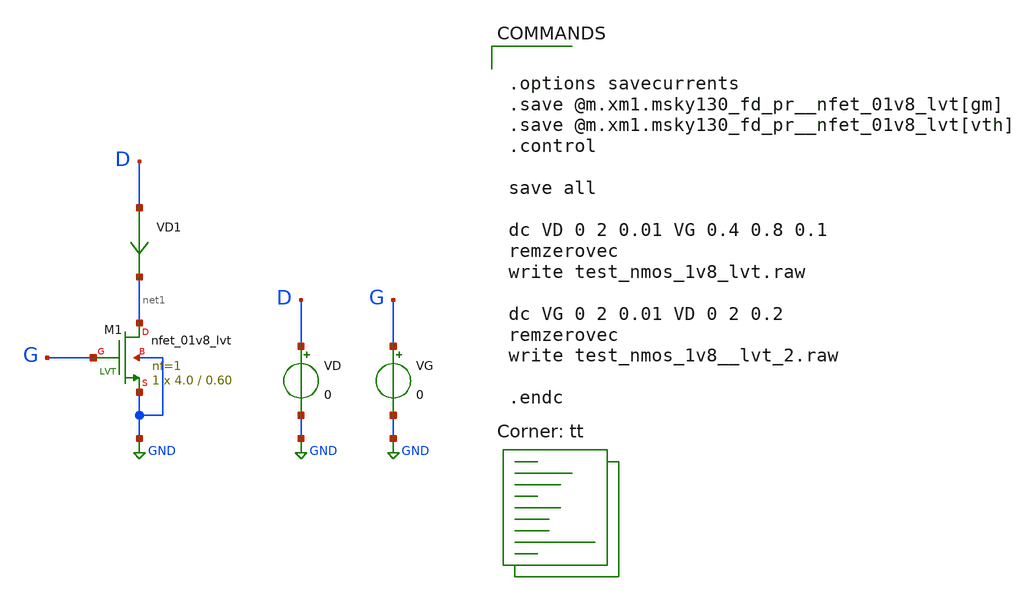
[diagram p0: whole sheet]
** sch_path: strongARM/test_nmos_1v8_lvt.sch
**.subckt test_nmos_1v8_lvt
VG G GND 0
VD D GND 0
VD1 D net1 0
.save i(vd1)
XM1 net1 G GND GND sky130_fd_pr__nfet_01v8_lvt L=0.60 W=4.0 nf=1 ad='int((nf+1)/2) * W/nf * 0.29' as='int((nf+2)/2) * W/nf * 0.29'
+ pd='2*int((nf+1)/2) * (W/nf + 0.29)' ps='2*int((nf+2)/2) * (W/nf + 0.29)' nrd='0.29 / W' nrs='0.29 / W'
+ sa=0 sb=0 sd=0 mult=1 m=1
**** begin user architecture code
.lib $::SKYWATER_MODELS/sky130.lib.spice tt


.options savecurrents
.save @m.xm1.msky130_fd_pr__nfet_01v8_lvt[gm]
.save @m.xm1.msky130_fd_pr__nfet_01v8_lvt[vth]
.control

save all

dc VD 0 2 0.01 VG 0.4 0.8 0.1
remzerovec
write test_nmos_1v8_lvt.raw

dc VG 0 2 0.01 VD 0 2 0.2
remzerovec
write test_nmos_1v8__lvt_2.raw

.endc


**** end user architecture code
**.ends
.GLOBAL GND
.end
